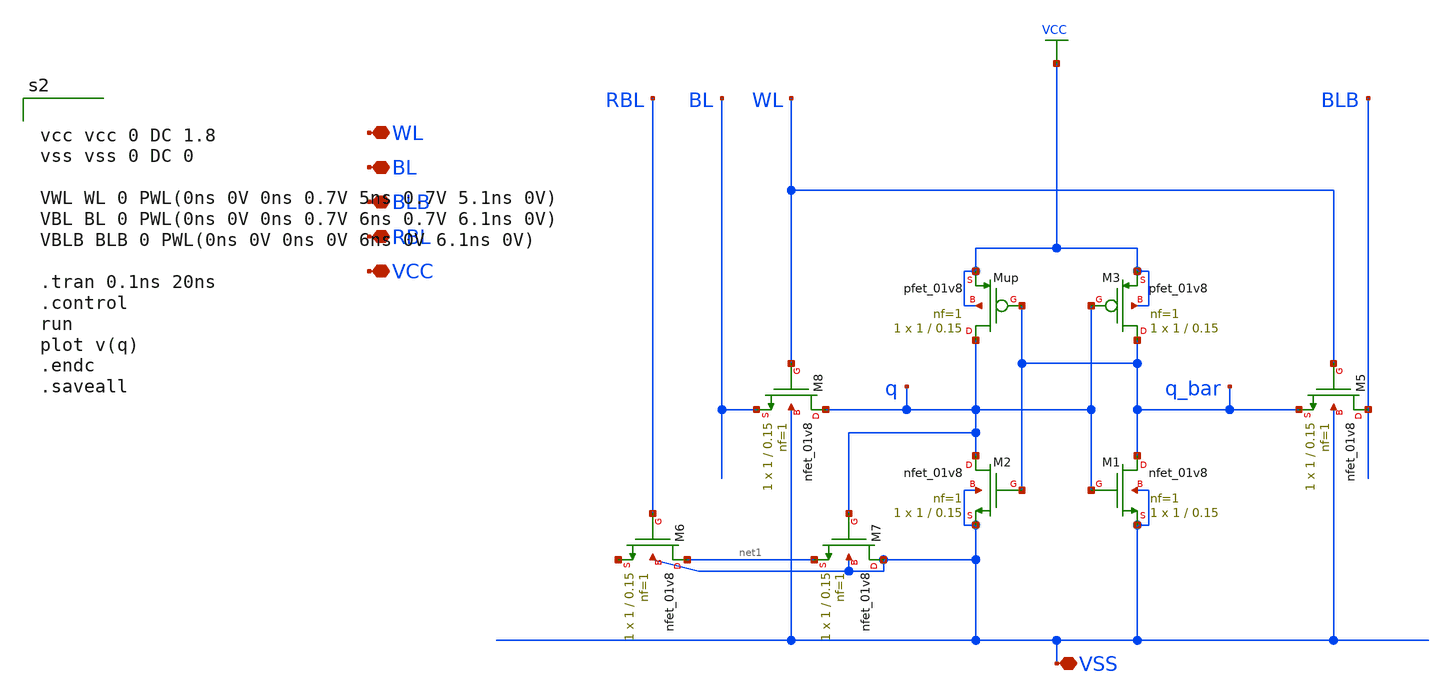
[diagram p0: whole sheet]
** sch_path: 8Tsram_old.sch
**.subckt 8Tsram_old WL BL BLB RBL VCC VSS
*.iopin WL
*.iopin BL
*.iopin BLB
*.iopin RBL
*.iopin VCC
*.iopin VSS
XM1 q_bar q VSS VSS sky130_fd_pr__nfet_01v8 L=0.15 W=1 nf=1 ad='int((1 + 1)/2) * 1 / 1 * 0.29' as='int((1 + 2)/2) * 1 / 1 * 0.29'
+ pd='2*int((1 + 1)/2) * (1 / 1 + 0.29)' ps='2*int((1 + 2)/2) * (1 / 1 + 0.29)' nrd='0.29 / 1 ' nrs='0.29 / 1 '
+ sa=0 sb=0 sd=0 mult=1 m=1
XM2 q q_bar VSS VSS sky130_fd_pr__nfet_01v8 L=0.15 W=1 nf=1 ad='int((1 + 1)/2) * 1 / 1 * 0.29' as='int((1 + 2)/2) * 1 / 1 * 0.29'
+ pd='2*int((1 + 1)/2) * (1 / 1 + 0.29)' ps='2*int((1 + 2)/2) * (1 / 1 + 0.29)' nrd='0.29 / 1 ' nrs='0.29 / 1 '
+ sa=0 sb=0 sd=0 mult=1 m=1
XM3 q_bar q VCC VCC sky130_fd_pr__pfet_01v8 L=0.15 W=1 nf=1 ad='int((1 + 1)/2) * 1 / 1 * 0.29' as='int((1 + 2)/2) * 1 / 1 * 0.29'
+ pd='2*int((1 + 1)/2) * (1 / 1 + 0.29)' ps='2*int((1 + 2)/2) * (1 / 1 + 0.29)' nrd='0.29 / 1 ' nrs='0.29 / 1 '
+ sa=0 sb=0 sd=0 mult=1 m=1
XMup q q_bar VCC VCC sky130_fd_pr__pfet_01v8 L=0.15 W=1 nf=1 ad='int((1 + 1)/2) * 1 / 1 * 0.29' as='int((1 + 2)/2) * 1 / 1 * 0.29'
+ pd='2*int((1 + 1)/2) * (1 / 1 + 0.29)' ps='2*int((1 + 2)/2) * (1 / 1 + 0.29)' nrd='0.29 / 1 ' nrs='0.29 / 1 '
+ sa=0 sb=0 sd=0 mult=1 m=1
XM5 BLB WL q_bar VSS sky130_fd_pr__nfet_01v8 L=0.15 W=1 nf=1 ad='int((1 + 1)/2) * 1 / 1 * 0.29' as='int((1 + 2)/2) * 1 / 1 * 0.29'
+ pd='2*int((1 + 1)/2) * (1 / 1 + 0.29)' ps='2*int((1 + 2)/2) * (1 / 1 + 0.29)' nrd='0.29 / 1 ' nrs='0.29 / 1 '
+ sa=0 sb=0 sd=0 mult=1 m=1
XM6 net1 RBL net2 VSS sky130_fd_pr__nfet_01v8 L=0.15 W=1 nf=1 ad='int((1 + 1)/2) * 1 / 1 * 0.29' as='int((1 + 2)/2) * 1 / 1 * 0.29'
+ pd='2*int((1 + 1)/2) * (1 / 1 + 0.29)' ps='2*int((1 + 2)/2) * (1 / 1 + 0.29)' nrd='0.29 / 1 ' nrs='0.29 / 1 '
+ sa=0 sb=0 sd=0 mult=1 m=1
XM7 VSS q net1 VSS sky130_fd_pr__nfet_01v8 L=0.15 W=1 nf=1 ad='int((1 + 1)/2) * 1 / 1 * 0.29' as='int((1 + 2)/2) * 1 / 1 * 0.29'
+ pd='2*int((1 + 1)/2) * (1 / 1 + 0.29)' ps='2*int((1 + 2)/2) * (1 / 1 + 0.29)' nrd='0.29 / 1 ' nrs='0.29 / 1 '
+ sa=0 sb=0 sd=0 mult=1 m=1
XM8 q WL BL VSS sky130_fd_pr__nfet_01v8 L=0.15 W=1 nf=1 ad='int((1 + 1)/2) * 1 / 1 * 0.29' as='int((1 + 2)/2) * 1 / 1 * 0.29'
+ pd='2*int((1 + 1)/2) * (1 / 1 + 0.29)' ps='2*int((1 + 2)/2) * (1 / 1 + 0.29)' nrd='0.29 / 1 ' nrs='0.29 / 1 '
+ sa=0 sb=0 sd=0 mult=1 m=1
**** begin user architecture code


vcc vcc 0 DC 1.8
vss vss 0 DC 0

VWL WL 0 PWL(0ns 0V 0ns 0.7V 5ns 0.7V 5.1ns 0V)
VBL BL 0 PWL(0ns 0V 0ns 0.7V 6ns 0.7V 6.1ns 0V)
VBLB BLB 0 PWL(0ns 0V 0ns 0V 6ns 0V 6.1ns 0V)

.tran 0.1ns 20ns
.control
run
plot v(q)
.endc
.saveall





**** end user architecture code
**.ends
.GLOBAL VCC
.end
